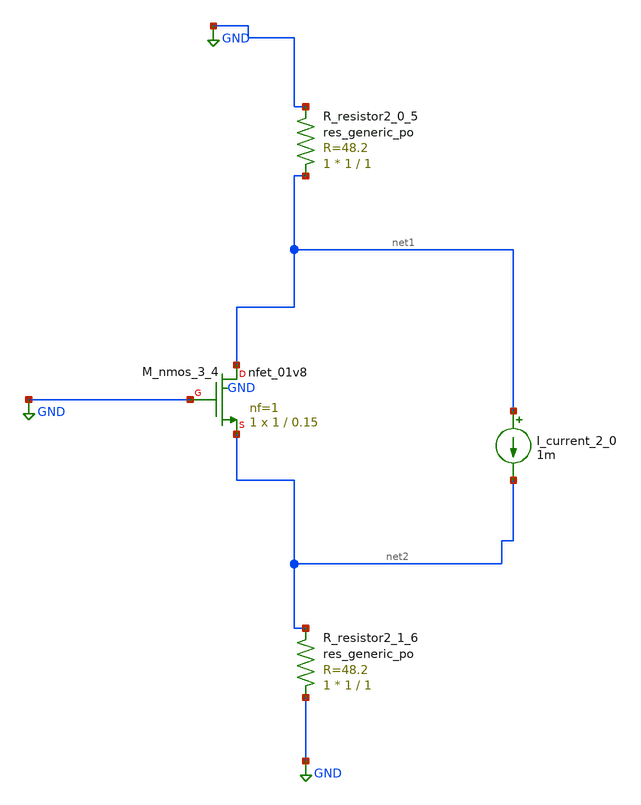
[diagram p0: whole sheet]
** sch_path: schematics/AMSNet/454.sch
**.subckt 454
I_current_2_0 net1 net2 1m
XM_nmos_3_4 net1 GND net2 GND sky130_fd_pr__nfet_01v8 L=0.15 W=1 nf=1 ad='int((1 + 1)/2) * 1 / 1 * 0.29'
+ as='int((1 + 2)/2) * 1 / 1 * 0.29' pd='2*int((1 + 1)/2) * (1 / 1 + 0.29)' ps='2*int((1 + 2)/2) * (1 / 1 + 0.29)'
+ nrd='0.29 / 1 ' nrs='0.29 / 1 ' sa=0 sb=0 sd=0 mult=1 m=1
XR_resistor2_0_5 net1 GND sky130_fd_pr__res_generic_po W=1 L=1 m=1
XR_resistor2_1_6 GND net2 sky130_fd_pr__res_generic_po W=1 L=1 m=1
**.ends
.GLOBAL GND
.end
